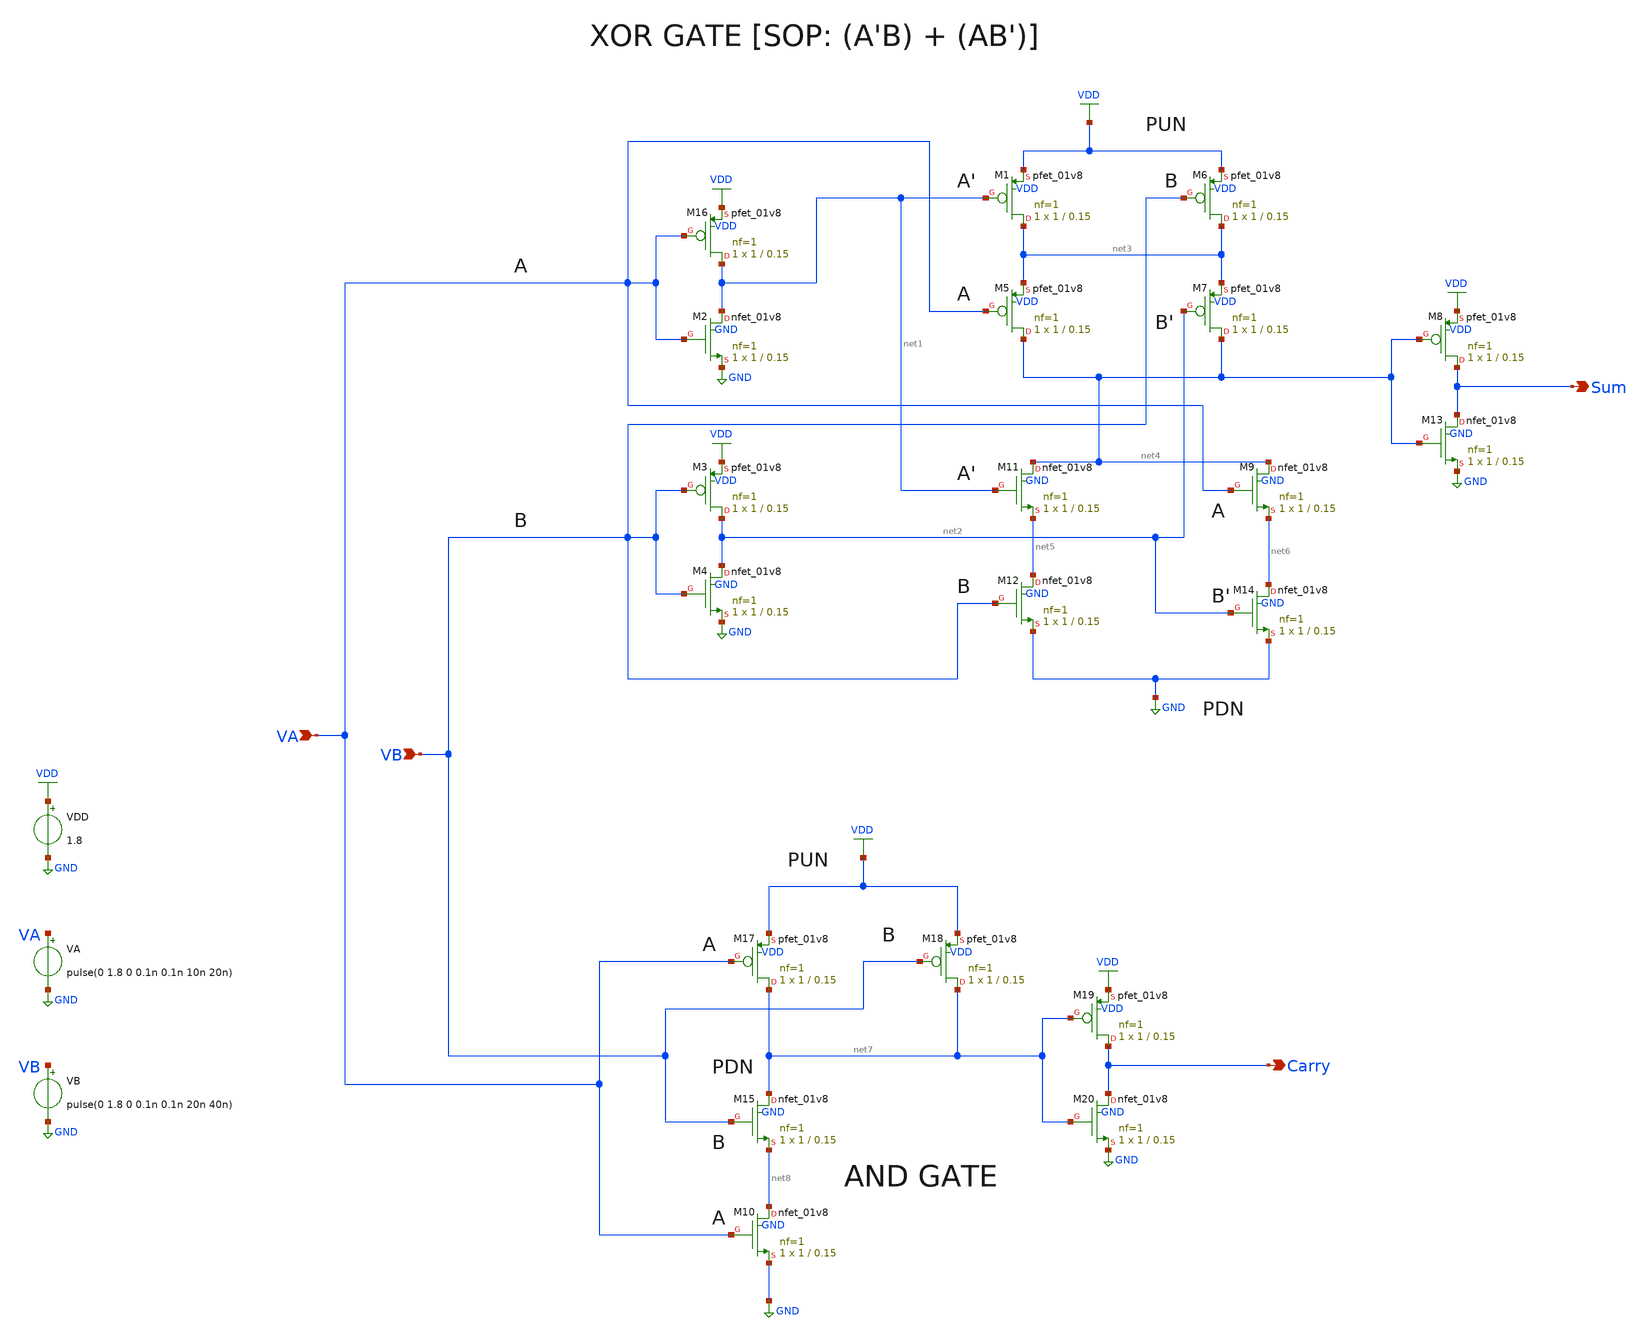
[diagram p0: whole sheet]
** sch_path: units/top/ana/blocks/half_adder/half_adder.sch
**.subckt half_adder VA VB Sum Carry
*.ipin VA
*.ipin VB
*.opin Sum
*.opin Carry
VB VB GND pulse(0 1.8 0 0.1n 0.1n 20n 40n)
VDD VDD GND 1.8
.save i(vdd)
VA VA GND pulse(0 1.8 0 0.1n 0.1n 10n 20n)
XM16 net1 VA VDD VDD sky130_fd_pr__pfet_01v8 L=0.15 W=1 nf=1 ad='int((1 + 1)/2) * 1 / 1 * 0.29' as='int((1 + 2)/2) * 1 / 1 * 0.29'
+ pd='2*int((1 + 1)/2) * (1 / 1 + 0.29)' ps='2*int((1 + 2)/2) * (1 / 1 + 0.29)' nrd='0.29 / 1 ' nrs='0.29 / 1 '
+ sa=0 sb=0 sd=0 mult=1 m=1
XM1 net3 net1 VDD VDD sky130_fd_pr__pfet_01v8 L=0.15 W=1 nf=1 ad='int((1 + 1)/2) * 1 / 1 * 0.29' as='int((1 + 2)/2) * 1 / 1 * 0.29'
+ pd='2*int((1 + 1)/2) * (1 / 1 + 0.29)' ps='2*int((1 + 2)/2) * (1 / 1 + 0.29)' nrd='0.29 / 1 ' nrs='0.29 / 1 '
+ sa=0 sb=0 sd=0 mult=1 m=1
XM5 net4 VA net3 VDD sky130_fd_pr__pfet_01v8 L=0.15 W=1 nf=1 ad='int((1 + 1)/2) * 1 / 1 * 0.29' as='int((1 + 2)/2) * 1 / 1 * 0.29'
+ pd='2*int((1 + 1)/2) * (1 / 1 + 0.29)' ps='2*int((1 + 2)/2) * (1 / 1 + 0.29)' nrd='0.29 / 1 ' nrs='0.29 / 1 '
+ sa=0 sb=0 sd=0 mult=1 m=1
XM6 net3 VB VDD VDD sky130_fd_pr__pfet_01v8 L=0.15 W=1 nf=1 ad='int((1 + 1)/2) * 1 / 1 * 0.29' as='int((1 + 2)/2) * 1 / 1 * 0.29'
+ pd='2*int((1 + 1)/2) * (1 / 1 + 0.29)' ps='2*int((1 + 2)/2) * (1 / 1 + 0.29)' nrd='0.29 / 1 ' nrs='0.29 / 1 '
+ sa=0 sb=0 sd=0 mult=1 m=1
XM7 net4 net2 net3 VDD sky130_fd_pr__pfet_01v8 L=0.15 W=1 nf=1 ad='int((1 + 1)/2) * 1 / 1 * 0.29' as='int((1 + 2)/2) * 1 / 1 * 0.29'
+ pd='2*int((1 + 1)/2) * (1 / 1 + 0.29)' ps='2*int((1 + 2)/2) * (1 / 1 + 0.29)' nrd='0.29 / 1 ' nrs='0.29 / 1 '
+ sa=0 sb=0 sd=0 mult=1 m=1
XM8 Sum net4 VDD VDD sky130_fd_pr__pfet_01v8 L=0.15 W=1 nf=1 ad='int((1 + 1)/2) * 1 / 1 * 0.29' as='int((1 + 2)/2) * 1 / 1 * 0.29'
+ pd='2*int((1 + 1)/2) * (1 / 1 + 0.29)' ps='2*int((1 + 2)/2) * (1 / 1 + 0.29)' nrd='0.29 / 1 ' nrs='0.29 / 1 '
+ sa=0 sb=0 sd=0 mult=1 m=1
XM3 net2 VB VDD VDD sky130_fd_pr__pfet_01v8 L=0.15 W=1 nf=1 ad='int((1 + 1)/2) * 1 / 1 * 0.29' as='int((1 + 2)/2) * 1 / 1 * 0.29'
+ pd='2*int((1 + 1)/2) * (1 / 1 + 0.29)' ps='2*int((1 + 2)/2) * (1 / 1 + 0.29)' nrd='0.29 / 1 ' nrs='0.29 / 1 '
+ sa=0 sb=0 sd=0 mult=1 m=1
XM4 net2 VB GND GND sky130_fd_pr__nfet_01v8 L=0.15 W=1 nf=1 ad='int((1 + 1)/2) * 1 / 1 * 0.29' as='int((1 + 2)/2) * 1 / 1 * 0.29'
+ pd='2*int((1 + 1)/2) * (1 / 1 + 0.29)' ps='2*int((1 + 2)/2) * (1 / 1 + 0.29)' nrd='0.29 / 1 ' nrs='0.29 / 1 '
+ sa=0 sb=0 sd=0 mult=1 m=1
XM2 net1 VA GND GND sky130_fd_pr__nfet_01v8 L=0.15 W=1 nf=1 ad='int((1 + 1)/2) * 1 / 1 * 0.29' as='int((1 + 2)/2) * 1 / 1 * 0.29'
+ pd='2*int((1 + 1)/2) * (1 / 1 + 0.29)' ps='2*int((1 + 2)/2) * (1 / 1 + 0.29)' nrd='0.29 / 1 ' nrs='0.29 / 1 '
+ sa=0 sb=0 sd=0 mult=1 m=1
XM12 net5 VB GND GND sky130_fd_pr__nfet_01v8 L=0.15 W=1 nf=1 ad='int((1 + 1)/2) * 1 / 1 * 0.29' as='int((1 + 2)/2) * 1 / 1 * 0.29'
+ pd='2*int((1 + 1)/2) * (1 / 1 + 0.29)' ps='2*int((1 + 2)/2) * (1 / 1 + 0.29)' nrd='0.29 / 1 ' nrs='0.29 / 1 '
+ sa=0 sb=0 sd=0 mult=1 m=1
XM11 net4 net1 net5 GND sky130_fd_pr__nfet_01v8 L=0.15 W=1 nf=1 ad='int((1 + 1)/2) * 1 / 1 * 0.29' as='int((1 + 2)/2) * 1 / 1 * 0.29'
+ pd='2*int((1 + 1)/2) * (1 / 1 + 0.29)' ps='2*int((1 + 2)/2) * (1 / 1 + 0.29)' nrd='0.29 / 1 ' nrs='0.29 / 1 '
+ sa=0 sb=0 sd=0 mult=1 m=1
XM9 net4 VA net6 GND sky130_fd_pr__nfet_01v8 L=0.15 W=1 nf=1 ad='int((1 + 1)/2) * 1 / 1 * 0.29' as='int((1 + 2)/2) * 1 / 1 * 0.29'
+ pd='2*int((1 + 1)/2) * (1 / 1 + 0.29)' ps='2*int((1 + 2)/2) * (1 / 1 + 0.29)' nrd='0.29 / 1 ' nrs='0.29 / 1 '
+ sa=0 sb=0 sd=0 mult=1 m=1
XM14 net6 net2 GND GND sky130_fd_pr__nfet_01v8 L=0.15 W=1 nf=1 ad='int((1 + 1)/2) * 1 / 1 * 0.29' as='int((1 + 2)/2) * 1 / 1 * 0.29'
+ pd='2*int((1 + 1)/2) * (1 / 1 + 0.29)' ps='2*int((1 + 2)/2) * (1 / 1 + 0.29)' nrd='0.29 / 1 ' nrs='0.29 / 1 '
+ sa=0 sb=0 sd=0 mult=1 m=1
XM13 Sum net4 GND GND sky130_fd_pr__nfet_01v8 L=0.15 W=1 nf=1 ad='int((1 + 1)/2) * 1 / 1 * 0.29' as='int((1 + 2)/2) * 1 / 1 * 0.29'
+ pd='2*int((1 + 1)/2) * (1 / 1 + 0.29)' ps='2*int((1 + 2)/2) * (1 / 1 + 0.29)' nrd='0.29 / 1 ' nrs='0.29 / 1 '
+ sa=0 sb=0 sd=0 mult=1 m=1
XM10 net8 VA GND GND sky130_fd_pr__nfet_01v8 L=0.15 W=1 nf=1 ad='int((1 + 1)/2) * 1 / 1 * 0.29' as='int((1 + 2)/2) * 1 / 1 * 0.29'
+ pd='2*int((1 + 1)/2) * (1 / 1 + 0.29)' ps='2*int((1 + 2)/2) * (1 / 1 + 0.29)' nrd='0.29 / 1 ' nrs='0.29 / 1 '
+ sa=0 sb=0 sd=0 mult=1 m=1
XM15 net7 VB net8 GND sky130_fd_pr__nfet_01v8 L=0.15 W=1 nf=1 ad='int((1 + 1)/2) * 1 / 1 * 0.29' as='int((1 + 2)/2) * 1 / 1 * 0.29'
+ pd='2*int((1 + 1)/2) * (1 / 1 + 0.29)' ps='2*int((1 + 2)/2) * (1 / 1 + 0.29)' nrd='0.29 / 1 ' nrs='0.29 / 1 '
+ sa=0 sb=0 sd=0 mult=1 m=1
XM17 net7 VA VDD VDD sky130_fd_pr__pfet_01v8 L=0.15 W=1 nf=1 ad='int((1 + 1)/2) * 1 / 1 * 0.29' as='int((1 + 2)/2) * 1 / 1 * 0.29'
+ pd='2*int((1 + 1)/2) * (1 / 1 + 0.29)' ps='2*int((1 + 2)/2) * (1 / 1 + 0.29)' nrd='0.29 / 1 ' nrs='0.29 / 1 '
+ sa=0 sb=0 sd=0 mult=1 m=1
XM18 net7 VB VDD VDD sky130_fd_pr__pfet_01v8 L=0.15 W=1 nf=1 ad='int((1 + 1)/2) * 1 / 1 * 0.29' as='int((1 + 2)/2) * 1 / 1 * 0.29'
+ pd='2*int((1 + 1)/2) * (1 / 1 + 0.29)' ps='2*int((1 + 2)/2) * (1 / 1 + 0.29)' nrd='0.29 / 1 ' nrs='0.29 / 1 '
+ sa=0 sb=0 sd=0 mult=1 m=1
XM19 Carry net7 VDD VDD sky130_fd_pr__pfet_01v8 L=0.15 W=1 nf=1 ad='int((1 + 1)/2) * 1 / 1 * 0.29' as='int((1 + 2)/2) * 1 / 1 * 0.29'
+ pd='2*int((1 + 1)/2) * (1 / 1 + 0.29)' ps='2*int((1 + 2)/2) * (1 / 1 + 0.29)' nrd='0.29 / 1 ' nrs='0.29 / 1 '
+ sa=0 sb=0 sd=0 mult=1 m=1
XM20 Carry net7 GND GND sky130_fd_pr__nfet_01v8 L=0.15 W=1 nf=1 ad='int((1 + 1)/2) * 1 / 1 * 0.29' as='int((1 + 2)/2) * 1 / 1 * 0.29'
+ pd='2*int((1 + 1)/2) * (1 / 1 + 0.29)' ps='2*int((1 + 2)/2) * (1 / 1 + 0.29)' nrd='0.29 / 1 ' nrs='0.29 / 1 '
+ sa=0 sb=0 sd=0 mult=1 m=1
**** begin user architecture code

.lib /usr/local/share/pdk/sky130B/libs.tech/ngspice/sky130.lib.spice tt
.option wnflag=1

 title: ="Inputs"
**** end user architecture code
**.ends
.GLOBAL VDD
.GLOBAL GND
**** begin user architecture code


.save v(VA) v(VB) v(Sum) v(Carry)
.tran 0.1n 200n


**** end user architecture code
.end
